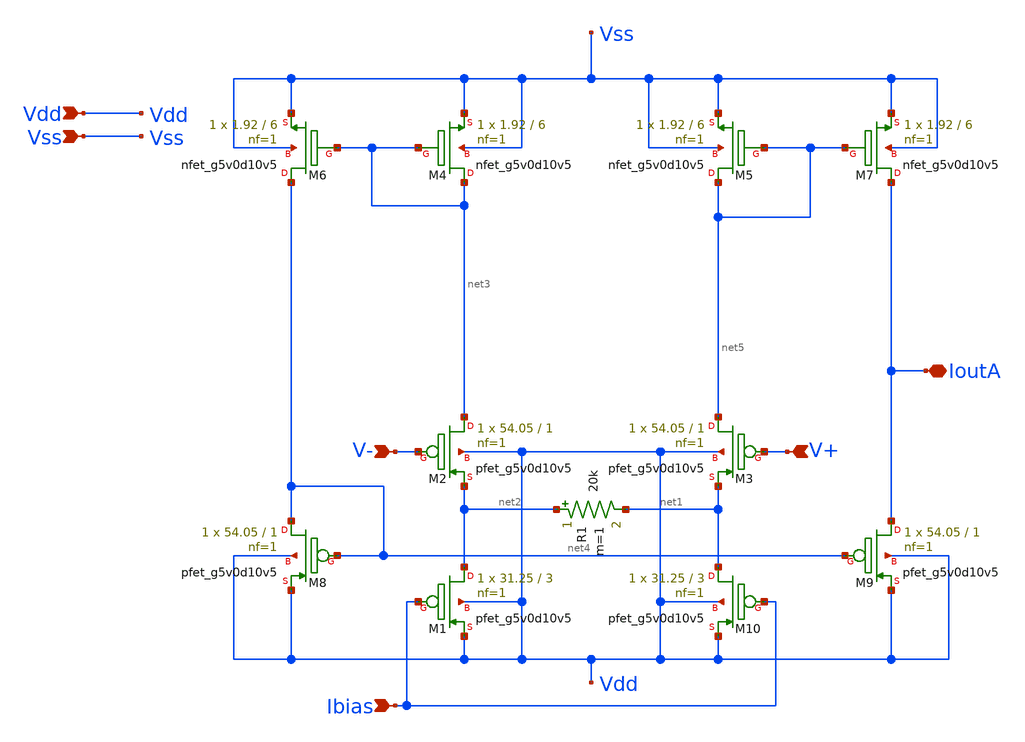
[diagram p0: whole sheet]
** sch_path: xschem/MIRROR_OTA.sch
**.subckt MIRROR_OTA V- V+ Vdd Vss Ibias IoutA
*.ipin V-
*.ipin V+
*.ipin Vdd
*.ipin Vss
*.ipin Ibias
*.iopin IoutA
XM1 net2 Ibias Vdd Vdd sky130_fd_pr__pfet_g5v0d10v5 L=3 W=31.25 nf=1 ad='int((1 + 1)/2) * 31.25 / 1 * 0.29'
+ as='int((1 + 2)/2) * 31.25 / 1 * 0.29' pd='2*int((1 + 1)/2) * (31.25 / 1 + 0.29)' ps='2*int((1 + 2)/2) * (31.25 / 1 + 0.29)'
+ nrd='0.29 / 31.25 ' nrs='0.29 / 31.25 ' sa=0 sb=0 sd=0 mult=1 m=1
XM2 net3 V- net2 Vdd sky130_fd_pr__pfet_g5v0d10v5 L=1 W=54.05 nf=1 ad='int((1 + 1)/2) * 54.05 / 1 * 0.29'
+ as='int((1 + 2)/2) * 54.05 / 1 * 0.29' pd='2*int((1 + 1)/2) * (54.05 / 1 + 0.29)' ps='2*int((1 + 2)/2) * (54.05 / 1 + 0.29)'
+ nrd='0.29 / 54.05 ' nrs='0.29 / 54.05 ' sa=0 sb=0 sd=0 mult=1 m=1
XM3 net5 V+ net1 Vdd sky130_fd_pr__pfet_g5v0d10v5 L=1 W=54.05 nf=1 ad='int((1 + 1)/2) * 54.05 / 1 * 0.29'
+ as='int((1 + 2)/2) * 54.05 / 1 * 0.29' pd='2*int((1 + 1)/2) * (54.05 / 1 + 0.29)' ps='2*int((1 + 2)/2) * (54.05 / 1 + 0.29)'
+ nrd='0.29 / 54.05 ' nrs='0.29 / 54.05 ' sa=0 sb=0 sd=0 mult=1 m=1
XM4 net3 net3 Vss Vss sky130_fd_pr__nfet_g5v0d10v5 L=6 W=1.92 nf=1 ad='int((1 + 1)/2) * 1.92 / 1 * 0.29'
+ as='int((1 + 2)/2) * 1.92 / 1 * 0.29' pd='2*int((1 + 1)/2) * (1.92 / 1 + 0.29)' ps='2*int((1 + 2)/2) * (1.92 / 1 + 0.29)'
+ nrd='0.29 / 1.92 ' nrs='0.29 / 1.92 ' sa=0 sb=0 sd=0 mult=1 m=1
XM5 net5 net5 Vss Vss sky130_fd_pr__nfet_g5v0d10v5 L=6 W=1.92 nf=1 ad='int((1 + 1)/2) * 1.92 / 1 * 0.29'
+ as='int((1 + 2)/2) * 1.92 / 1 * 0.29' pd='2*int((1 + 1)/2) * (1.92 / 1 + 0.29)' ps='2*int((1 + 2)/2) * (1.92 / 1 + 0.29)'
+ nrd='0.29 / 1.92 ' nrs='0.29 / 1.92 ' sa=0 sb=0 sd=0 mult=1 m=1
XM6 net4 net3 Vss Vss sky130_fd_pr__nfet_g5v0d10v5 L=6 W=1.92 nf=1 ad='int((1 + 1)/2) * 1.92 / 1 * 0.29'
+ as='int((1 + 2)/2) * 1.92 / 1 * 0.29' pd='2*int((1 + 1)/2) * (1.92 / 1 + 0.29)' ps='2*int((1 + 2)/2) * (1.92 / 1 + 0.29)'
+ nrd='0.29 / 1.92 ' nrs='0.29 / 1.92 ' sa=0 sb=0 sd=0 mult=1 m=1
XM7 IoutA net5 Vss Vss sky130_fd_pr__nfet_g5v0d10v5 L=6 W=1.92 nf=1 ad='int((1 + 1)/2) * 1.92 / 1 * 0.29'
+ as='int((1 + 2)/2) * 1.92 / 1 * 0.29' pd='2*int((1 + 1)/2) * (1.92 / 1 + 0.29)' ps='2*int((1 + 2)/2) * (1.92 / 1 + 0.29)'
+ nrd='0.29 / 1.92 ' nrs='0.29 / 1.92 ' sa=0 sb=0 sd=0 mult=1 m=1
XM8 net4 net4 Vdd Vdd sky130_fd_pr__pfet_g5v0d10v5 L=1 W=54.05 nf=1 ad='int((1 + 1)/2) * 54.05 / 1 * 0.29'
+ as='int((1 + 2)/2) * 54.05 / 1 * 0.29' pd='2*int((1 + 1)/2) * (54.05 / 1 + 0.29)' ps='2*int((1 + 2)/2) * (54.05 / 1 + 0.29)'
+ nrd='0.29 / 54.05 ' nrs='0.29 / 54.05 ' sa=0 sb=0 sd=0 mult=1 m=1
XM9 IoutA net4 Vdd Vdd sky130_fd_pr__pfet_g5v0d10v5 L=1 W=54.05 nf=1 ad='int((1 + 1)/2) * 54.05 / 1 * 0.29'
+ as='int((1 + 2)/2) * 54.05 / 1 * 0.29' pd='2*int((1 + 1)/2) * (54.05 / 1 + 0.29)' ps='2*int((1 + 2)/2) * (54.05 / 1 + 0.29)'
+ nrd='0.29 / 54.05 ' nrs='0.29 / 54.05 ' sa=0 sb=0 sd=0 mult=1 m=1
XM10 net1 Ibias Vdd Vdd sky130_fd_pr__pfet_g5v0d10v5 L=3 W=31.25 nf=1 ad='int((1 + 1)/2) * 31.25 / 1 * 0.29'
+ as='int((1 + 2)/2) * 31.25 / 1 * 0.29' pd='2*int((1 + 1)/2) * (31.25 / 1 + 0.29)' ps='2*int((1 + 2)/2) * (31.25 / 1 + 0.29)'
+ nrd='0.29 / 31.25 ' nrs='0.29 / 31.25 ' sa=0 sb=0 sd=0 mult=1 m=1
R1 net2 net1 20k m=1
**.ends
.end
